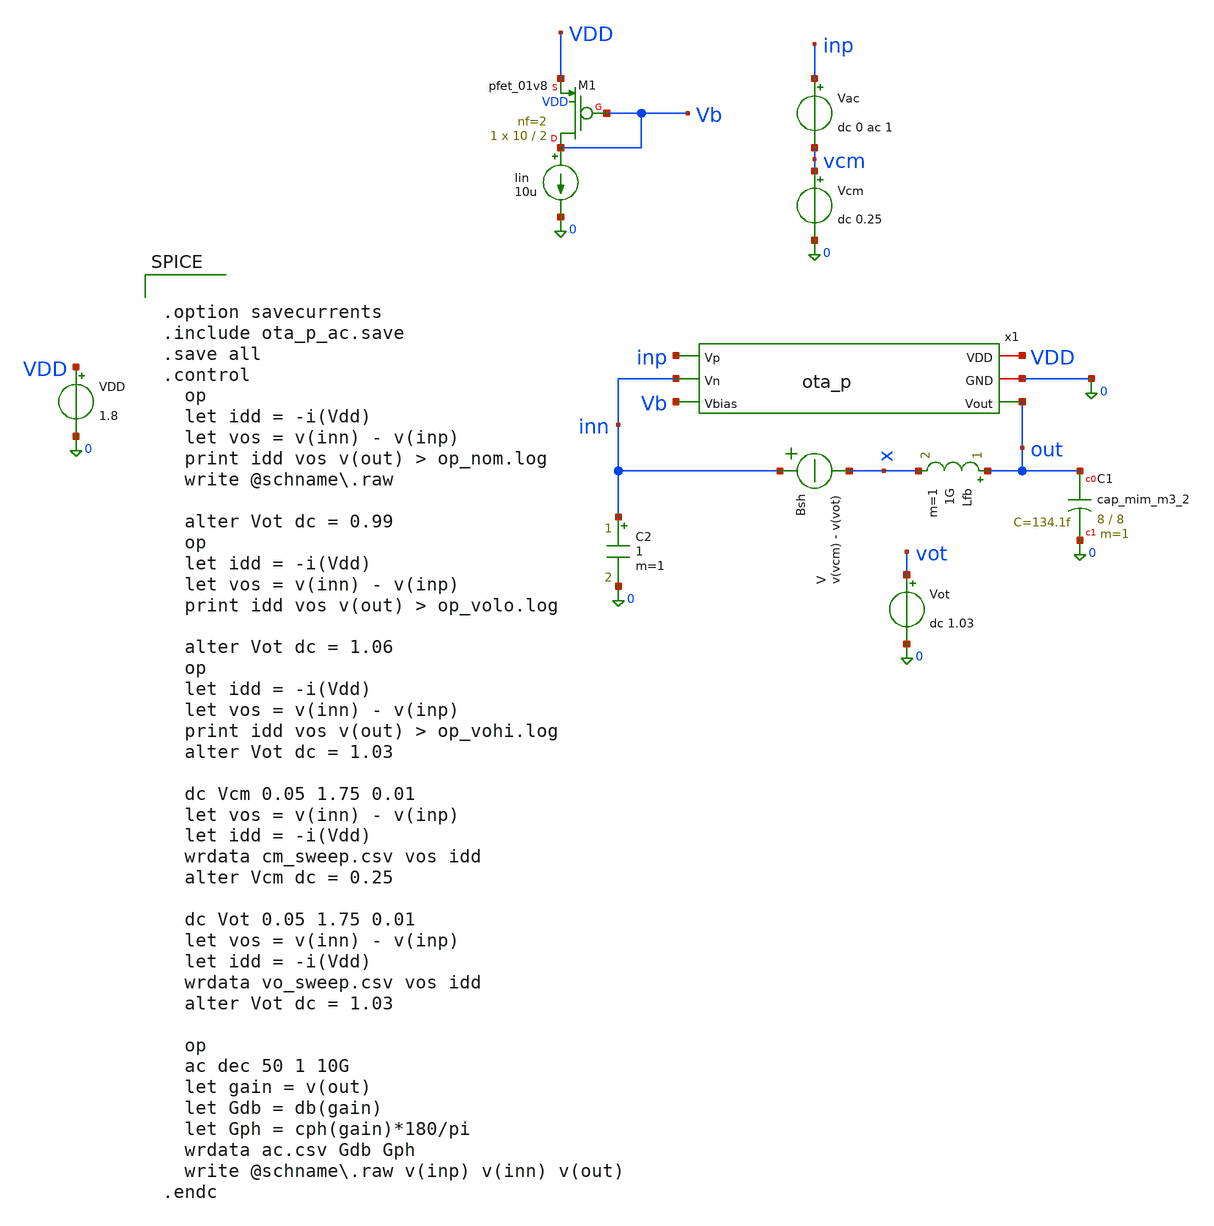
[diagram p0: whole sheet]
** sch_path: sch/cascode/ota_p_ac.sch
**.subckt ota_p_ac
Iin Vb 0 10u
VDD VDD 0 1.8
.save i(vdd)
XM1 Vb Vb VDD VDD sky130_fd_pr__pfet_01v8 L=2 W=10 nf=2 ad='int((2 + 1)/2) * 10 / 2 * 0.29' as='int((2 + 2)/2) * 10 / 2 * 0.29'
+ pd='2*int((2 + 1)/2) * (10 / 2 + 0.29)' ps='2*int((2 + 2)/2) * (10 / 2 + 0.29)' nrd='0.29 / 10 ' nrs='0.29 / 10 '
+ sa=0 sb=0 sd=0 mult=1 m=1
x1 VDD 0 Vb inp inn out ota_p
Lfb out x 1G m=1
Bsh inn x V = v(vcm) - v(vot)
Vcm vcm 0 dc 0.25
.save i(vcm)
Vac inp vcm dc 0 ac 1
.save i(vac)
Vot vot 0 dc 1.03
.save i(vot)
XC1 out 0 sky130_fd_pr__cap_mim_m3_2 W=8 L=8 MF=1 m=1
C2 inn 0 1 m=1
**** begin user architecture code

** opencircuitdesign pdks install
.lib $::SKYWATER_MODELS/sky130.lib.spice tt
.include $::SKYWATER_STDCELLS/sky130_fd_sc_hd.spice



.option savecurrents
.include ota_p_ac.save
.save all
.control
  op
  let idd = -i(Vdd)
  let vos = v(inn) - v(inp)
  print idd vos v(out) > op_nom.log
  write @schname\.raw

  alter Vot dc = 0.99
  op
  let idd = -i(Vdd)
  let vos = v(inn) - v(inp)
  print idd vos v(out) > op_volo.log

  alter Vot dc = 1.06
  op
  let idd = -i(Vdd)
  let vos = v(inn) - v(inp)
  print idd vos v(out) > op_vohi.log
  alter Vot dc = 1.03

  dc Vcm 0.05 1.75 0.01
  let vos = v(inn) - v(inp)
  let idd = -i(Vdd)
  wrdata cm_sweep.csv vos idd
  alter Vcm dc = 0.25

  dc Vot 0.05 1.75 0.01
  let vos = v(inn) - v(inp)
  let idd = -i(Vdd)
  wrdata vo_sweep.csv vos idd
  alter Vot dc = 1.03

  op
  ac dec 50 1 10G
  let gain = v(out)
  let Gdb = db(gain)
  let Gph = cph(gain)*180/pi
  wrdata ac.csv Gdb Gph
  write @schname\.raw v(inp) v(inn) v(out)
.endc


**** end user architecture code
**.ends

* expanding   symbol:  /foss/designs/sar_adc/sch/cascode/ota_p.sym # of pins=6
** sym_path: sch/cascode/ota_p.sym
** sch_path: sch/cascode/ota_p.sch
.subckt ota_p VDD GND Vbias Vp Vn Vout
*.ipin Vbias
*.opin Vout
*.iopin VDD
*.iopin GND
*.ipin Vp
*.ipin Vn
XM1 net1 Vp Vx VDD sky130_fd_pr__pfet_01v8 L=2 W=25 nf=5 ad='int((5 + 1)/2) * 25 / 5 * 0.29' as='int((5 + 2)/2) * 25 / 5 * 0.29'
+ pd='2*int((5 + 1)/2) * (25 / 5 + 0.29)' ps='2*int((5 + 2)/2) * (25 / 5 + 0.29)' nrd='0.29 / 25 ' nrs='0.29 / 25 '
+ sa=0 sb=0 sd=0 mult=1 m=1
XM2 Vout Vn Vx VDD sky130_fd_pr__pfet_01v8 L=2 W=25 nf=5 ad='int((5 + 1)/2) * 25 / 5 * 0.29' as='int((5 + 2)/2) * 25 / 5 * 0.29'
+ pd='2*int((5 + 1)/2) * (25 / 5 + 0.29)' ps='2*int((5 + 2)/2) * (25 / 5 + 0.29)' nrd='0.29 / 25 ' nrs='0.29 / 25 '
+ sa=0 sb=0 sd=0 mult=1 m=1
XM3 net1 net1 GND GND sky130_fd_pr__nfet_01v8 L=2 W=1.5 nf=1 ad='int((1 + 1)/2) * 1.5 / 1 * 0.29' as='int((1 + 2)/2) * 1.5 / 1 * 0.29'
+ pd='2*int((1 + 1)/2) * (1.5 / 1 + 0.29)' ps='2*int((1 + 2)/2) * (1.5 / 1 + 0.29)' nrd='0.29 / 1.5 ' nrs='0.29 / 1.5 '
+ sa=0 sb=0 sd=0 mult=1 m=1
XM4 Vout net1 GND GND sky130_fd_pr__nfet_01v8 L=2 W=1.5 nf=1 ad='int((1 + 1)/2) * 1.5 / 1 * 0.29' as='int((1 + 2)/2) * 1.5 / 1 * 0.29'
+ pd='2*int((1 + 1)/2) * (1.5 / 1 + 0.29)' ps='2*int((1 + 2)/2) * (1.5 / 1 + 0.29)' nrd='0.29 / 1.5 ' nrs='0.29 / 1.5 '
+ sa=0 sb=0 sd=0 mult=1 m=1
XM5 Vx Vbias VDD VDD sky130_fd_pr__pfet_01v8 L=2 W=10 nf=2 ad='int((2 + 1)/2) * 10 / 2 * 0.29' as='int((2 + 2)/2) * 10 / 2 * 0.29'
+ pd='2*int((2 + 1)/2) * (10 / 2 + 0.29)' ps='2*int((2 + 2)/2) * (10 / 2 + 0.29)' nrd='0.29 / 10 ' nrs='0.29 / 10 '
+ sa=0 sb=0 sd=0 mult=1 m=1
.ends

.end
